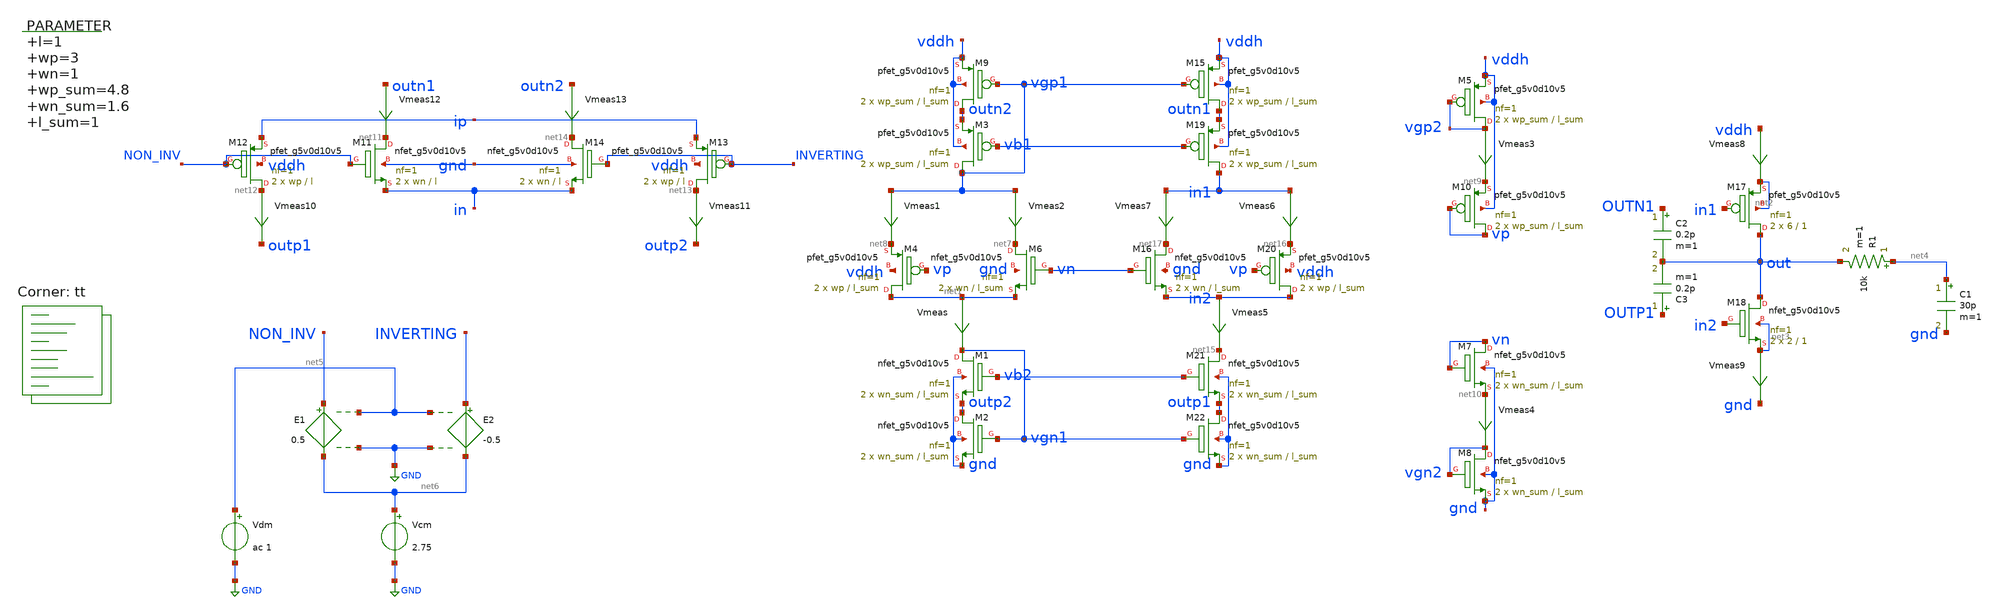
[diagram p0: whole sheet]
** sch_path: xschem/op_amp_output_stage.sch
**.subckt op_amp_output_stage
Vmeas net1 vgn1 0
.save i(vmeas)
XM9 outn2 vgp1 vddh vddh sky130_fd_pr__pfet_g5v0d10v5 L=l_sum W=wp_sum nf=1 ad='int((nf+1)/2) * W/nf * 0.29'
+ as='int((nf+2)/2) * W/nf * 0.29' pd='2*int((nf+1)/2) * (W/nf + 0.29)' ps='2*int((nf+2)/2) * (W/nf + 0.29)'
+ nrd='0.29 / W' nrs='0.29 / W' sa=0 sb=0 sd=0 mult=2 m=2
XM6 net7 vn net1 gnd sky130_fd_pr__nfet_g5v0d10v5 L=l_sum W=wn nf=1 ad='int((nf+1)/2) * W/nf * 0.29'
+ as='int((nf+2)/2) * W/nf * 0.29' pd='2*int((nf+1)/2) * (W/nf + 0.29)' ps='2*int((nf+2)/2) * (W/nf + 0.29)'
+ nrd='0.29 / W' nrs='0.29 / W' sa=0 sb=0 sd=0 mult=2 m=2
Vmeas1 vgp1 net8 0
.save i(vmeas1)
Vmeas2 vgp1 net7 0
.save i(vmeas2)
Vmeas3 vgp2 net9 0
.save i(vmeas3)
Vmeas4 net10 vgn2 0
.save i(vmeas4)
XM4 net1 vp net8 vddh sky130_fd_pr__pfet_g5v0d10v5 L=l_sum W=wp nf=1 ad='int((nf+1)/2) * W/nf * 0.29'
+ as='int((nf+2)/2) * W/nf * 0.29' pd='2*int((nf+1)/2) * (W/nf + 0.29)' ps='2*int((nf+2)/2) * (W/nf + 0.29)'
+ nrd='0.29 / W' nrs='0.29 / W' sa=0 sb=0 sd=0 mult=2 m=2
XM5 vgp2 vgp2 vddh vddh sky130_fd_pr__pfet_g5v0d10v5 L=l_sum W=wp_sum nf=1 ad='int((nf+1)/2) * W/nf * 0.29'
+ as='int((nf+2)/2) * W/nf * 0.29' pd='2*int((nf+1)/2) * (W/nf + 0.29)' ps='2*int((nf+2)/2) * (W/nf + 0.29)'
+ nrd='0.29 / W' nrs='0.29 / W' sa=0 sb=0 sd=0 mult=2 m=2
XM1 vgn1 vb2 outp2 gnd sky130_fd_pr__nfet_g5v0d10v5 L=l_sum W=wn_sum nf=1 ad='int((nf+1)/2) * W/nf * 0.29'
+ as='int((nf+2)/2) * W/nf * 0.29' pd='2*int((nf+1)/2) * (W/nf + 0.29)' ps='2*int((nf+2)/2) * (W/nf + 0.29)'
+ nrd='0.29 / W' nrs='0.29 / W' sa=0 sb=0 sd=0 mult=2 m=2
XM7 vn vn net10 gnd sky130_fd_pr__nfet_g5v0d10v5 L=l_sum W=wn_sum nf=1 ad='int((nf+1)/2) * W/nf * 0.29'
+ as='int((nf+2)/2) * W/nf * 0.29' pd='2*int((nf+1)/2) * (W/nf + 0.29)' ps='2*int((nf+2)/2) * (W/nf + 0.29)'
+ nrd='0.29 / W' nrs='0.29 / W' sa=0 sb=0 sd=0 mult=2 m=2
XM8 vgn2 vgn2 gnd gnd sky130_fd_pr__nfet_g5v0d10v5 L=l_sum W=wn_sum nf=1 ad='int((nf+1)/2) * W/nf * 0.29'
+ as='int((nf+2)/2) * W/nf * 0.29' pd='2*int((nf+1)/2) * (W/nf + 0.29)' ps='2*int((nf+2)/2) * (W/nf + 0.29)'
+ nrd='0.29 / W' nrs='0.29 / W' sa=0 sb=0 sd=0 mult=2 m=2
.param l=1 wp=3 wn=1 wp_sum=4.8 wn_sum=1.6 l_sum=1
XM17 out in1 net2 net2 sky130_fd_pr__pfet_g5v0d10v5 L=1 W=6 nf=1 ad='int((nf+1)/2) * W/nf * 0.29' as='int((nf+2)/2) * W/nf * 0.29'
+ pd='2*int((nf+1)/2) * (W/nf + 0.29)' ps='2*int((nf+2)/2) * (W/nf + 0.29)' nrd='0.29 / W' nrs='0.29 / W'
+ sa=0 sb=0 sd=0 mult=2 m=2
XM18 out in2 net3 net3 sky130_fd_pr__nfet_g5v0d10v5 L=1 W=2 nf=1 ad='int((nf+1)/2) * W/nf * 0.29' as='int((nf+2)/2) * W/nf * 0.29'
+ pd='2*int((nf+1)/2) * (W/nf + 0.29)' ps='2*int((nf+2)/2) * (W/nf + 0.29)' nrd='0.29 / W' nrs='0.29 / W'
+ sa=0 sb=0 sd=0 mult=2 m=2
Vmeas8 vddh net2 0
.save i(vmeas8)
Vmeas9 net3 gnd 0
.save i(vmeas9)
C1 net4 gnd 30p m=1
XM11 net11 NON_INV in gnd sky130_fd_pr__nfet_g5v0d10v5 L=l W=wn nf=1 ad='int((nf+1)/2) * W/nf * 0.29'
+ as='int((nf+2)/2) * W/nf * 0.29' pd='2*int((nf+1)/2) * (W/nf + 0.29)' ps='2*int((nf+2)/2) * (W/nf + 0.29)'
+ nrd='0.29 / W' nrs='0.29 / W' sa=0 sb=0 sd=0 mult=2 m=2
XM12 net12 NON_INV ip vddh sky130_fd_pr__pfet_g5v0d10v5 L=l W=wp nf=1 ad='int((nf+1)/2) * W/nf * 0.29'
+ as='int((nf+2)/2) * W/nf * 0.29' pd='2*int((nf+1)/2) * (W/nf + 0.29)' ps='2*int((nf+2)/2) * (W/nf + 0.29)'
+ nrd='0.29 / W' nrs='0.29 / W' sa=0 sb=0 sd=0 mult=2 m=2
XM13 net13 INVERTING ip vddh sky130_fd_pr__pfet_g5v0d10v5 L=l W=wp nf=1 ad='int((nf+1)/2) * W/nf * 0.29'
+ as='int((nf+2)/2) * W/nf * 0.29' pd='2*int((nf+1)/2) * (W/nf + 0.29)' ps='2*int((nf+2)/2) * (W/nf + 0.29)'
+ nrd='0.29 / W' nrs='0.29 / W' sa=0 sb=0 sd=0 mult=2 m=2
XM14 net14 INVERTING in gnd sky130_fd_pr__nfet_g5v0d10v5 L=l W=wn nf=1 ad='int((nf+1)/2) * W/nf * 0.29'
+ as='int((nf+2)/2) * W/nf * 0.29' pd='2*int((nf+1)/2) * (W/nf + 0.29)' ps='2*int((nf+2)/2) * (W/nf + 0.29)'
+ nrd='0.29 / W' nrs='0.29 / W' sa=0 sb=0 sd=0 mult=2 m=2
Vmeas5 in2 net15 0
.save i(vmeas5)
Vmeas6 in1 net16 0
.save i(vmeas6)
Vmeas7 in1 net17 0
.save i(vmeas7)
Vmeas10 net12 outp1 0
.save i(vmeas10)
Vmeas11 net13 outp2 0
.save i(vmeas11)
Vmeas12 outn1 net11 0
.save i(vmeas12)
Vmeas13 outn2 net14 0
.save i(vmeas13)
C2 OUTN1 out 0.2p m=1
C3 OUTP1 out 0.2p m=1
R1 net4 out 10k m=1
XM3 vgp1 vb1 outn2 vddh sky130_fd_pr__pfet_g5v0d10v5 L=l_sum W=wp_sum nf=1 ad='int((nf+1)/2) * W/nf * 0.29'
+ as='int((nf+2)/2) * W/nf * 0.29' pd='2*int((nf+1)/2) * (W/nf + 0.29)' ps='2*int((nf+2)/2) * (W/nf + 0.29)'
+ nrd='0.29 / W' nrs='0.29 / W' sa=0 sb=0 sd=0 mult=2 m=2
XM15 outn1 vgp1 vddh vddh sky130_fd_pr__pfet_g5v0d10v5 L=l_sum W=wp_sum nf=1 ad='int((nf+1)/2) * W/nf * 0.29'
+ as='int((nf+2)/2) * W/nf * 0.29' pd='2*int((nf+1)/2) * (W/nf + 0.29)' ps='2*int((nf+2)/2) * (W/nf + 0.29)'
+ nrd='0.29 / W' nrs='0.29 / W' sa=0 sb=0 sd=0 mult=2 m=2
XM19 in1 vb1 outn1 vddh sky130_fd_pr__pfet_g5v0d10v5 L=l_sum W=wp_sum nf=1 ad='int((nf+1)/2) * W/nf * 0.29'
+ as='int((nf+2)/2) * W/nf * 0.29' pd='2*int((nf+1)/2) * (W/nf + 0.29)' ps='2*int((nf+2)/2) * (W/nf + 0.29)'
+ nrd='0.29 / W' nrs='0.29 / W' sa=0 sb=0 sd=0 mult=2 m=2
XM2 outp2 vgn1 gnd gnd sky130_fd_pr__nfet_g5v0d10v5 L=l_sum W=wn_sum nf=1 ad='int((nf+1)/2) * W/nf * 0.29'
+ as='int((nf+2)/2) * W/nf * 0.29' pd='2*int((nf+1)/2) * (W/nf + 0.29)' ps='2*int((nf+2)/2) * (W/nf + 0.29)'
+ nrd='0.29 / W' nrs='0.29 / W' sa=0 sb=0 sd=0 mult=2 m=2
XM21 net15 vb2 outp1 gnd sky130_fd_pr__nfet_g5v0d10v5 L=l_sum W=wn_sum nf=1 ad='int((nf+1)/2) * W/nf * 0.29'
+ as='int((nf+2)/2) * W/nf * 0.29' pd='2*int((nf+1)/2) * (W/nf + 0.29)' ps='2*int((nf+2)/2) * (W/nf + 0.29)'
+ nrd='0.29 / W' nrs='0.29 / W' sa=0 sb=0 sd=0 mult=2 m=2
XM22 outp1 vgn1 gnd gnd sky130_fd_pr__nfet_g5v0d10v5 L=l_sum W=wn_sum nf=1 ad='int((nf+1)/2) * W/nf * 0.29'
+ as='int((nf+2)/2) * W/nf * 0.29' pd='2*int((nf+1)/2) * (W/nf + 0.29)' ps='2*int((nf+2)/2) * (W/nf + 0.29)'
+ nrd='0.29 / W' nrs='0.29 / W' sa=0 sb=0 sd=0 mult=2 m=2
XM20 in2 vp net16 vddh sky130_fd_pr__pfet_g5v0d10v5 L=l_sum W=wp nf=1 ad='int((nf+1)/2) * W/nf * 0.29'
+ as='int((nf+2)/2) * W/nf * 0.29' pd='2*int((nf+1)/2) * (W/nf + 0.29)' ps='2*int((nf+2)/2) * (W/nf + 0.29)'
+ nrd='0.29 / W' nrs='0.29 / W' sa=0 sb=0 sd=0 mult=2 m=2
XM16 net17 vn in2 gnd sky130_fd_pr__nfet_g5v0d10v5 L=l_sum W=wn nf=1 ad='int((nf+1)/2) * W/nf * 0.29'
+ as='int((nf+2)/2) * W/nf * 0.29' pd='2*int((nf+1)/2) * (W/nf + 0.29)' ps='2*int((nf+2)/2) * (W/nf + 0.29)'
+ nrd='0.29 / W' nrs='0.29 / W' sa=0 sb=0 sd=0 mult=2 m=2
XM10 vp vp net9 vddh sky130_fd_pr__pfet_g5v0d10v5 L=l_sum W=wp_sum nf=1 ad='int((nf+1)/2) * W/nf * 0.29'
+ as='int((nf+2)/2) * W/nf * 0.29' pd='2*int((nf+1)/2) * (W/nf + 0.29)' ps='2*int((nf+2)/2) * (W/nf + 0.29)'
+ nrd='0.29 / W' nrs='0.29 / W' sa=0 sb=0 sd=0 mult=2 m=2
E1 NON_INV net6 net5 GND 0.5
E2 INVERTING net6 net5 GND -0.5
Vdm net5 GND ac 1
Vcm net6 GND 2.75
**** begin user architecture code
.lib $::SKYWATER_MODELS/sky130.lib.spice tt



  .option wnflag=1
  .option safecurrents
  ********************Static Current Sources***************************
  Ivp vp gnd 200n
  Ivn vddh vn 200n
  Iip vddh ip 40n
  Iin in gnd 40n
  ********************Static Voltage Sources***************************
  Vddh vddh gnd dc 5.5

  vb1 vb1 gnd dc 4.3687
  vb2 vb2 gnd dc 0.9587
  ********************Dynamic Voltage Sources***************************
  *******Calculation**********
  .param base_f=100e3 base_t={1/base_f} base_th={base_t/2} base_d={base_th}
  .param d2_th ={base_th} d2_t={2*d2_th}
  .param d1_th ={4*d2_th} d1_t={d0_th}
  .param d0_th ={4*d1_th} d0_t={4*d0_th}

  .param d20_d ={0} d21_d={1*d2_th} d22_d={2*d2_th} d23_d={3*d2_th}
  .param d10_d ={0} d11_d={1*d1_th} d12_d={2*d1_th} d13_d={3*d1_th}
  .param d00_d ={0} d01_d={1*d0_th} d02_d={2*d0_th} d03_d={3*d0_th}
  *******Signals**********
  .param vhi=5.5
  Vin1 b[0] gnd pulse(0 {vhi} {0} 1p 1p {10u} {20u})
*  Vin2 b[1] gnd pulse(0 {vhi} {0} 1p 1p {20u} {40u})
*  vin1 inx gnd sin({5.5/2} {5.5/2} 100k)
*  vin2 iny gnd sin({5.5/2} {-5.5/2} 100k)
  ********************Simulation Commands*****************************
  .control
     reset
     save all

     *dc vin 0 5.5 0.001
     *dc Iy 0 1u 0.001u
     *tran 1n 50u
     ac dec 100 1 10MEG

     let vout_mag =abs(v(out))
     let vout_phase_margin = phase(v(out))*180/pi + 180
     meas ac Aol find vout_mag at = 10
     meas ac UGF when vout_mag=1 fall=1
     meas ac PM find vout_phase_margin when vout_mag=1

     write output_stage-tb.raw
     set appendwrite
*    quit 0
  .endc



**** end user architecture code
**.ends
.GLOBAL GND
.end
